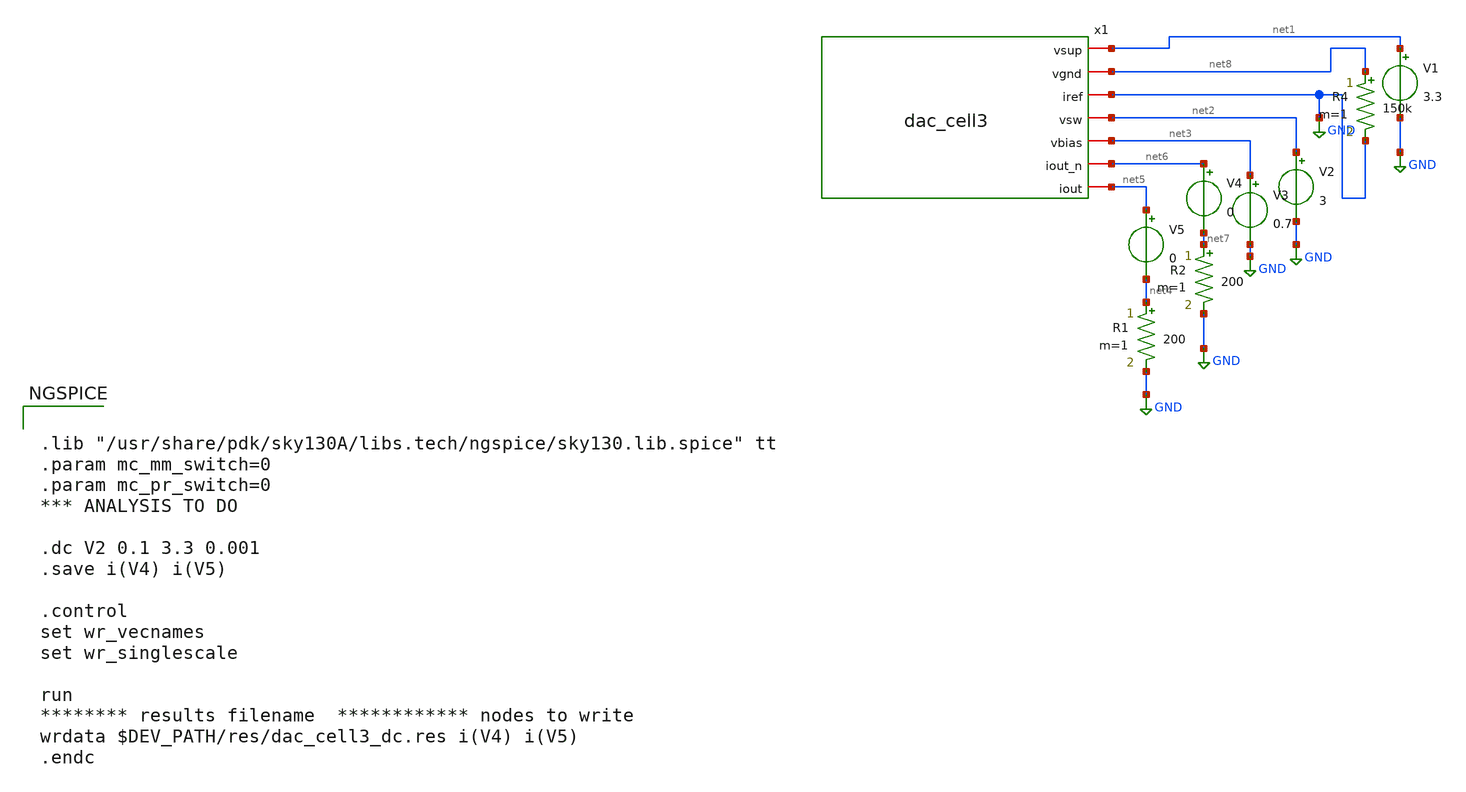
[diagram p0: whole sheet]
** sch_path: dev/dac_cell3/tb/tb_dac_cell3_dc.sch
**.subckt tb_dac_cell3_dc
V1 net1 GND 3.3
V2 net2 GND 3
V3 net3 GND 0.7
V4 net6 net7 0
V5 net5 net4 0
R1 net4 GND 200 m=1
R2 net7 GND 200 m=1
R4 net8 GND 150k m=1
x1 net1 net8 GND net2 net3 net6 net5 dac_cell3
**** begin user architecture code


.lib "/usr/share/pdk/sky130A/libs.tech/ngspice/sky130.lib.spice" tt
.param mc_mm_switch=0
.param mc_pr_switch=0
*** ANALYSIS TO DO

.dc V2 0.1 3.3 0.001
.save i(V4) i(V5)

.control
set wr_vecnames
set wr_singlescale

run
******** results filename  ************ nodes to write
wrdata $DEV_PATH/res/dac_cell3_dc.res i(V4) i(V5)
.endc


**** end user architecture code
**.ends

* expanding   symbol:  dac_cell3.sym # of pins=7
** sym_path: dev/dac_cell3/tb/dac_cell3.sym
** sch_path: dev/dac_cell3/tb/dac_cell3.sch
.subckt dac_cell3 vsup vgnd iref vsw vbias iout_n iout
*.iopin vsup
*.iopin vgnd
*.iopin iref
*.iopin vsw
*.iopin iout
*.iopin iout_n
*.iopin vbias
XM1 iref iref vsup vsup sky130_fd_pr__pfet_g5v0d10v5 L=1 W=1 nf=1 ad='int((nf+1)/2) * W/nf * 0.29' as='int((nf+2)/2) * W/nf * 0.29'
+ pd='2*int((nf+1)/2) * (W/nf + 0.29)' ps='2*int((nf+2)/2) * (W/nf + 0.29)' nrd='0.29 / W' nrs='0.29 / W'
+ sa=0 sb=0 sd=0 mult=1 m=1
XM2 sourceM3M4 iref sourceM2 vsup sky130_fd_pr__pfet_g5v0d10v5 L=1 W=4 nf=1 ad='int((nf+1)/2) * W/nf * 0.29'
+ as='int((nf+2)/2) * W/nf * 0.29' pd='2*int((nf+1)/2) * (W/nf + 0.29)' ps='2*int((nf+2)/2) * (W/nf + 0.29)'
+ nrd='0.29 / W' nrs='0.29 / W' sa=0 sb=0 sd=0 mult=1 m=1
XM3 iout vsw sourceM3M4 vsup sky130_fd_pr__pfet_g5v0d10v5 L=1 W=4 nf=1 ad='int((nf+1)/2) * W/nf * 0.29'
+ as='int((nf+2)/2) * W/nf * 0.29' pd='2*int((nf+1)/2) * (W/nf + 0.29)' ps='2*int((nf+2)/2) * (W/nf + 0.29)'
+ nrd='0.29 / W' nrs='0.29 / W' sa=0 sb=0 sd=0 mult=1 m=1
XM4 iout_n vbias sourceM3M4 vsup sky130_fd_pr__pfet_g5v0d10v5 L=1 W=4 nf=1 ad='int((nf+1)/2) * W/nf * 0.29'
+ as='int((nf+2)/2) * W/nf * 0.29' pd='2*int((nf+1)/2) * (W/nf + 0.29)' ps='2*int((nf+2)/2) * (W/nf + 0.29)'
+ nrd='0.29 / W' nrs='0.29 / W' sa=0 sb=0 sd=0 mult=1 m=1
XR1 parR vsup vgnd sky130_fd_pr__res_xhigh_po_0p69 L=13 mult=1 m=1
XR2 sourceM2 parR vgnd sky130_fd_pr__res_xhigh_po_0p69 L=13 mult=1 m=1
XR3 parR vsup vgnd sky130_fd_pr__res_xhigh_po_0p69 L=13 mult=1 m=1
XR4 sourceM2 parR vgnd sky130_fd_pr__res_xhigh_po_0p69 L=13 mult=1 m=1
.ends

.GLOBAL GND
.end
